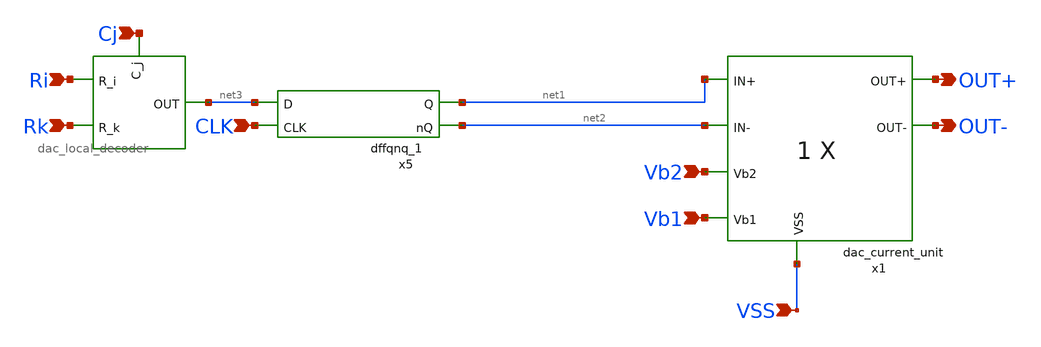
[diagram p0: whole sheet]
** sch_path: DAC/xschem/dac_current_cell_16X.sch
**.subckt dac_current_cell_16X VSS OUT+ OUT- Vb2 Vb1 CLK Ri Rk Cj
*.ipin VSS
*.opin OUT+
*.opin OUT-
*.ipin Vb2
*.ipin Vb1
*.ipin CLK
*.ipin Ri
*.ipin Rk
*.ipin Cj
x1 OUT+ OUT- net1 net2 Vb2 Vb1 VSS dac_current_unit nf=1
x3 Cj Rk Ri net3 DVDD DVNW DVPW DVSS dac_local_decoder
x5 net3 net1 CLK net2 DVDD DVNW DVPW DVSS dffqnq_1
**.ends
.end
